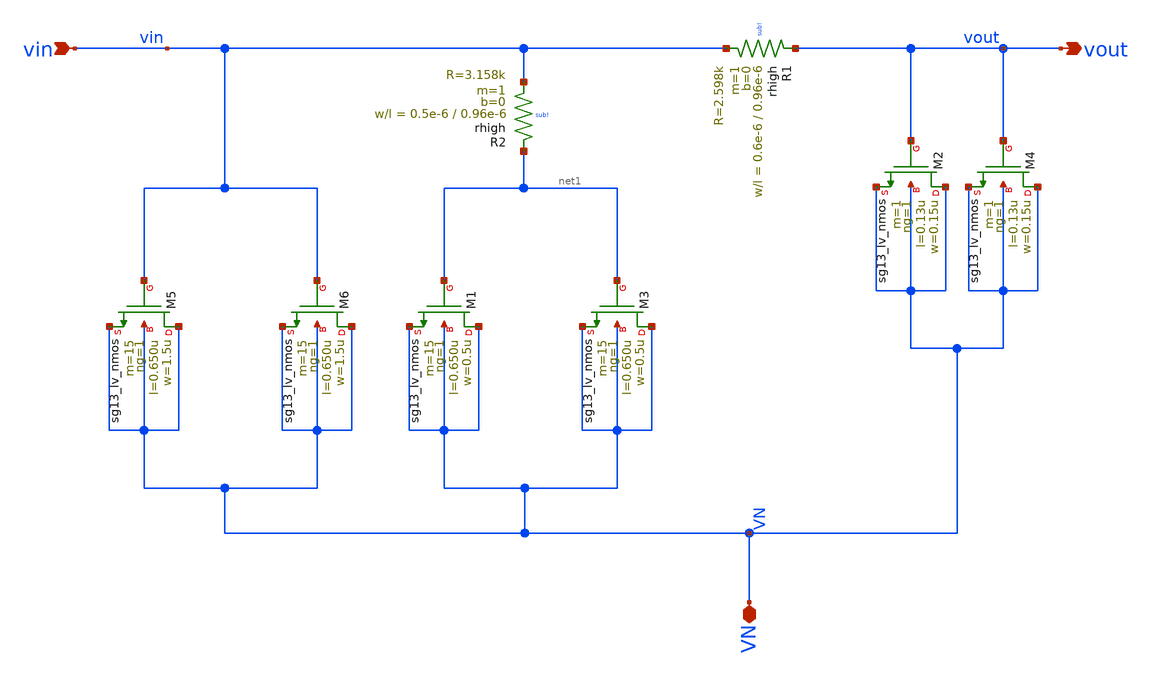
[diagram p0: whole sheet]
** sch_path: 30_MHz_Fractional_N_PLL/design_data/xschem/LOOP_FILTER.sch
**.subckt LOOP_FILTER VN vin vout
*.iopin VN
*.ipin vin
*.opin vout
XR1 vout vin sub! rhigh w=0.6e-6 l=0.96e-6 m=1 b=0 mm_ok=1
XM1 VN net1 VN VN sg13_lv_nmos w=0.5u l=0.650u ng=1 m=15 mm_ok=1
XM2 VN vout VN VN sg13_lv_nmos w=0.15u l=0.13u ng=1 m=1 mm_ok=1
XM3 VN net1 VN VN sg13_lv_nmos w=0.5u l=0.650u ng=1 m=15 mm_ok=1
XM4 VN vout VN VN sg13_lv_nmos w=0.15u l=0.13u ng=1 m=1 mm_ok=1
XR2 net1 vin sub! rhigh w=0.5e-6 l=0.96e-6 m=1 b=0 mm_ok=1
XM5 VN vin VN VN sg13_lv_nmos w=1.5u l=0.650u ng=1 m=15 mm_ok=1
XM6 VN vin VN VN sg13_lv_nmos w=1.5u l=0.650u ng=1 m=15 mm_ok=1
**.ends
.end
